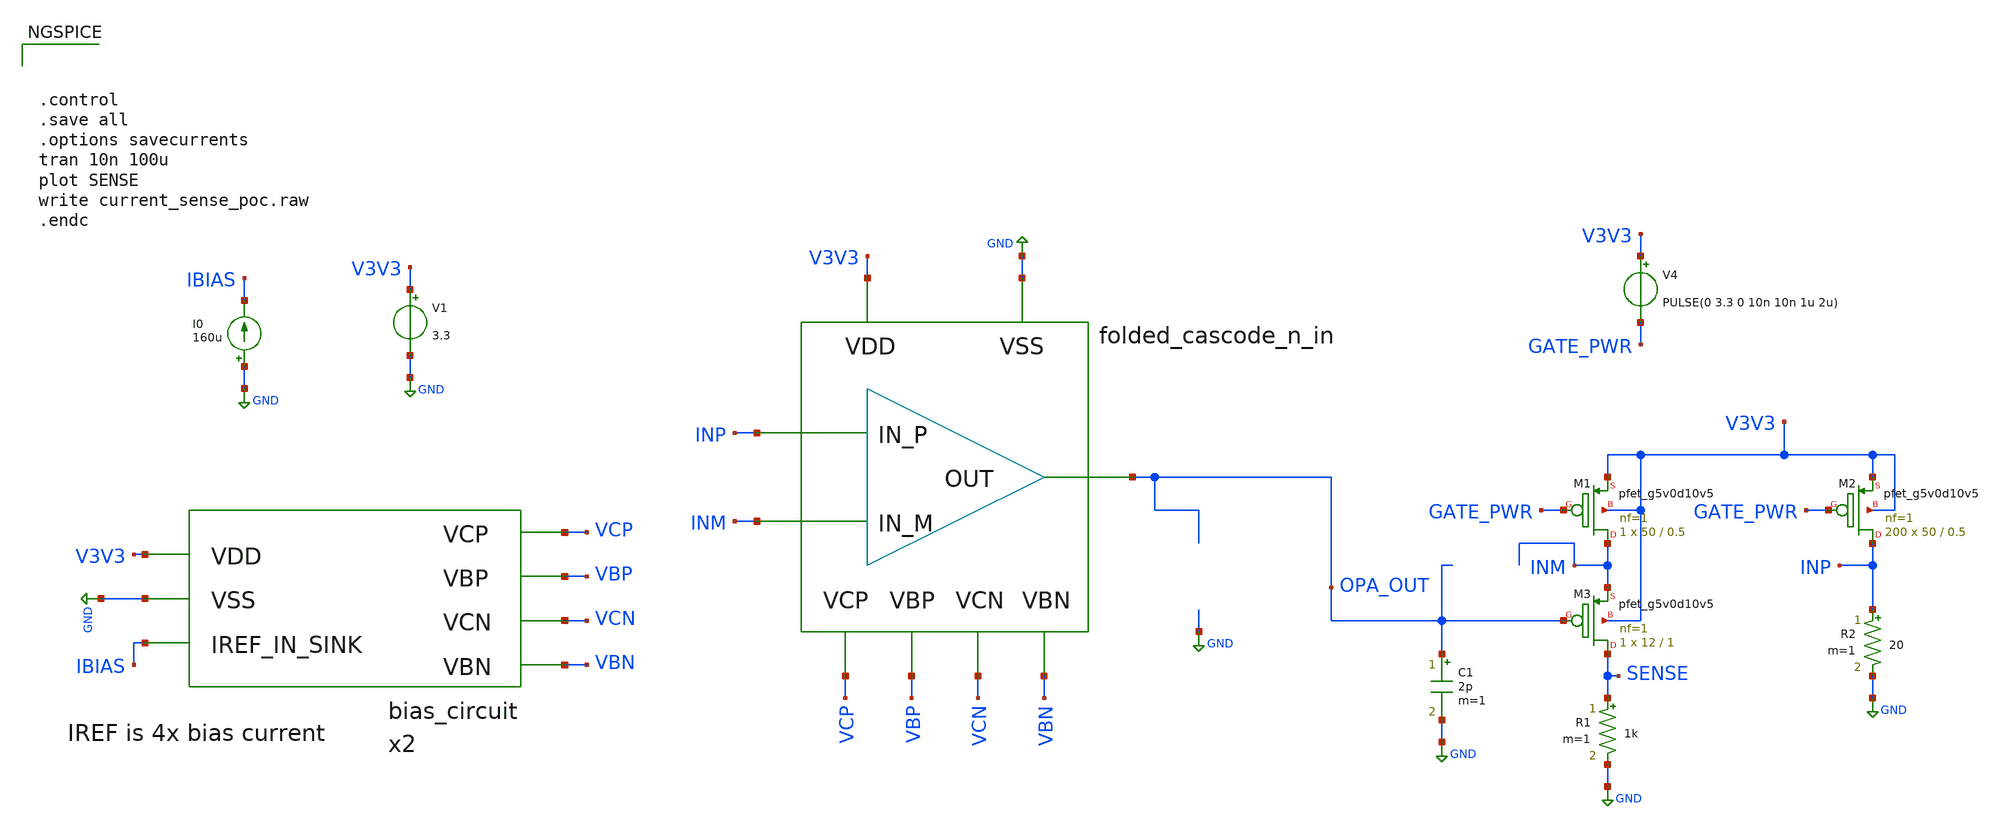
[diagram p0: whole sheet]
** sch_path: design/current-sense/current_sense_poc.sch
**.subckt current_sense_poc
V1 V3V3 GND 3.3
I0 GND IBIAS 160u
x2 V3V3 GND VCP VBP VCN VBN IBIAS bias_circuit
XM1 INM GATE_PWR V3V3 V3V3 sky130_fd_pr__pfet_g5v0d10v5 L=0.5 W=50 nf=1 ad='int((nf+1)/2) * W/nf * 0.29'
+ as='int((nf+2)/2) * W/nf * 0.29' pd='2*int((nf+1)/2) * (W/nf + 0.29)' ps='2*int((nf+2)/2) * (W/nf + 0.29)'
+ nrd='0.29 / W' nrs='0.29 / W' sa=0 sb=0 sd=0 mult=1 m=1
XM2 INP GATE_PWR V3V3 V3V3 sky130_fd_pr__pfet_g5v0d10v5 L=0.5 W=50 nf=1 ad='int((nf+1)/2) * W/nf * 0.29'
+ as='int((nf+2)/2) * W/nf * 0.29' pd='2*int((nf+1)/2) * (W/nf + 0.29)' ps='2*int((nf+2)/2) * (W/nf + 0.29)'
+ nrd='0.29 / W' nrs='0.29 / W' sa=0 sb=0 sd=0 mult=200 m=200
V4 V3V3 GATE_PWR PULSE(0 3.3 0 10n 10n 1u 2u)
XM3 SENSE OPA_OUT INM V3V3 sky130_fd_pr__pfet_g5v0d10v5 L=1 W=12 nf=1 ad='int((nf+1)/2) * W/nf * 0.29'
+ as='int((nf+2)/2) * W/nf * 0.29' pd='2*int((nf+1)/2) * (W/nf + 0.29)' ps='2*int((nf+2)/2) * (W/nf + 0.29)'
+ nrd='0.29 / W' nrs='0.29 / W' sa=0 sb=0 sd=0 mult=1 m=1
R1 SENSE GND 1k m=1
R2 INP GND 20 m=1
C1 OPA_OUT GND 2p m=1
**** begin user architecture code



.control
.save all
.options savecurrents
tran 10n 100u
plot SENSE
write current_sense_poc.raw
.endc



.include $::SKYWATER_MODELS/cells/nfet_01v8/sky130_fd_pr__nfet_01v8__tt.corner.spice
.include $::SKYWATER_MODELS/cells/nfet_01v8_lvt/sky130_fd_pr__nfet_01v8_lvt__tt.corner.spice
.include $::SKYWATER_MODELS/cells/pfet_01v8/sky130_fd_pr__pfet_01v8__tt.corner.spice
.include $::SKYWATER_MODELS/cells/nfet_03v3_nvt/sky130_fd_pr__nfet_03v3_nvt__tt.corner.spice
.include $::SKYWATER_MODELS/cells/nfet_05v0_nvt/sky130_fd_pr__nfet_05v0_nvt__tt.corner.spice
.include $::SKYWATER_MODELS/cells/esd_nfet_01v8/sky130_fd_pr__esd_nfet_01v8__tt.corner.spice
.include $::SKYWATER_MODELS/cells/pfet_01v8_lvt/sky130_fd_pr__pfet_01v8_lvt__tt.corner.spice
.include $::SKYWATER_MODELS/cells/pfet_01v8_hvt/sky130_fd_pr__pfet_01v8_hvt__tt.corner.spice
.include $::SKYWATER_MODELS/cells/esd_pfet_g5v0d10v5/sky130_fd_pr__esd_pfet_g5v0d10v5__tt.corner.spice
.include $::SKYWATER_MODELS/cells/pfet_g5v0d10v5/sky130_fd_pr__pfet_g5v0d10v5__tt.corner.spice
.include $::SKYWATER_MODELS/cells/pfet_g5v0d16v0/sky130_fd_pr__pfet_g5v0d16v0__tt.corner.spice
.include $::SKYWATER_MODELS/cells/nfet_g5v0d10v5/sky130_fd_pr__nfet_g5v0d10v5__tt.corner.spice
.include $::SKYWATER_MODELS/cells/nfet_g5v0d16v0/sky130_fd_pr__nfet_g5v0d16v0__tt_discrete.corner.spice
.include $::SKYWATER_MODELS/cells/esd_nfet_g5v0d10v5/sky130_fd_pr__esd_nfet_g5v0d10v5__tt.corner.spice
.include $::SKYWATER_MODELS/models/corners/tt/nonfet.spice
* Mismatch parameters
.include $::SKYWATER_MODELS/cells/nfet_01v8/sky130_fd_pr__nfet_01v8__mismatch.corner.spice
.include $::SKYWATER_MODELS/cells/pfet_01v8/sky130_fd_pr__pfet_01v8__mismatch.corner.spice
.include $::SKYWATER_MODELS/cells/nfet_01v8_lvt/sky130_fd_pr__nfet_01v8_lvt__mismatch.corner.spice
.include $::SKYWATER_MODELS/cells/pfet_01v8_lvt/sky130_fd_pr__pfet_01v8_lvt__mismatch.corner.spice
.include $::SKYWATER_MODELS/cells/pfet_01v8_hvt/sky130_fd_pr__pfet_01v8_hvt__mismatch.corner.spice
.include $::SKYWATER_MODELS/cells/nfet_g5v0d10v5/sky130_fd_pr__nfet_g5v0d10v5__mismatch.corner.spice
.include $::SKYWATER_MODELS/cells/pfet_g5v0d10v5/sky130_fd_pr__pfet_g5v0d10v5__mismatch.corner.spice
.include $::SKYWATER_MODELS/cells/nfet_05v0_nvt/sky130_fd_pr__nfet_05v0_nvt__mismatch.corner.spice
.include $::SKYWATER_MODELS/cells/nfet_03v3_nvt/sky130_fd_pr__nfet_03v3_nvt__mismatch.corner.spice
* Resistor$::SKYWATER_MODELS/Capacitor
.include $::SKYWATER_MODELS/models/r+c/res_typical__cap_typical.spice
.include $::SKYWATER_MODELS/models/r+c/res_typical__cap_typical__lin.spice
* Special cells
.include $::SKYWATER_MODELS/models/corners/tt/specialized_cells.spice
* All models
.include $::SKYWATER_MODELS/models/all.spice
* Corner
.include $::SKYWATER_MODELS/models/corners/tt/rf.spice

**** end user architecture code
**.ends

* expanding   symbol:  /home/wbraun/projects/open-pmic/design/bias-circuit/bias_circuit.sym # of
*+ pins=7
** sym_path: design/bias-circuit/bias_circuit.sym
** sch_path: design/bias-circuit/bias_circuit.sch
.subckt bias_circuit VDD VSS VCP VBP VCN VBN IREF_IN_SINK
*.ipin IREF_IN_SINK
*.ipin VCN
*.ipin VSS
*.ipin VDD
*.ipin VCP
*.ipin VBP
*.ipin VBN
XM2 VBP VBP VDD VDD sky130_fd_pr__pfet_g5v0d10v5 L=1 W=12 nf=1 ad='int((nf+1)/2) * W/nf * 0.29' as='int((nf+2)/2) * W/nf * 0.29'
+ pd='2*int((nf+1)/2) * (W/nf + 0.29)' ps='2*int((nf+2)/2) * (W/nf + 0.29)' nrd='0.29 / W' nrs='0.29 / W'
+ sa=0 sb=0 sd=0 mult=1 m=1
XM3 net1 VBP VDD VDD sky130_fd_pr__pfet_g5v0d10v5 L=5 W=12 nf=1 ad='int((nf+1)/2) * W/nf * 0.29' as='int((nf+2)/2) * W/nf * 0.29'
+ pd='2*int((nf+1)/2) * (W/nf + 0.29)' ps='2*int((nf+2)/2) * (W/nf + 0.29)' nrd='0.29 / W' nrs='0.29 / W'
+ sa=0 sb=0 sd=0 mult=1 m=1
XM4 VCN VBP VDD VDD sky130_fd_pr__pfet_g5v0d10v5 L=1 W=12 nf=1 ad='int((nf+1)/2) * W/nf * 0.29' as='int((nf+2)/2) * W/nf * 0.29'
+ pd='2*int((nf+1)/2) * (W/nf + 0.29)' ps='2*int((nf+2)/2) * (W/nf + 0.29)' nrd='0.29 / W' nrs='0.29 / W'
+ sa=0 sb=0 sd=0 mult=1 m=1
XM5 net1 net1 net2 VSS sky130_fd_pr__nfet_g5v0d10v5 L=1 W=12 nf=1 ad='int((nf+1)/2) * W/nf * 0.29' as='int((nf+2)/2) * W/nf * 0.29'
+ pd='2*int((nf+1)/2) * (W/nf + 0.29)' ps='2*int((nf+2)/2) * (W/nf + 0.29)' nrd='0.29 / W' nrs='0.29 / W'
+ sa=0 sb=0 sd=0 mult=4 m=4
XM6 net2 net1 VSS VSS sky130_fd_pr__nfet_g5v0d10v5 L=1 W=12 nf=1 ad='int((nf+1)/2) * W/nf * 0.29' as='int((nf+2)/2) * W/nf * 0.29'
+ pd='2*int((nf+1)/2) * (W/nf + 0.29)' ps='2*int((nf+2)/2) * (W/nf + 0.29)' nrd='0.29 / W' nrs='0.29 / W'
+ sa=0 sb=0 sd=0 mult=1 m=1
XM7 VCN VCN net2 VSS sky130_fd_pr__nfet_g5v0d10v5 L=1 W=12 nf=1 ad='int((nf+1)/2) * W/nf * 0.29' as='int((nf+2)/2) * W/nf * 0.29'
+ pd='2*int((nf+1)/2) * (W/nf + 0.29)' ps='2*int((nf+2)/2) * (W/nf + 0.29)' nrd='0.29 / W' nrs='0.29 / W'
+ sa=0 sb=0 sd=0 mult=1 m=1
XM8 VBN VBN VSS VSS sky130_fd_pr__nfet_g5v0d10v5 L=1 W=12 nf=1 ad='int((nf+1)/2) * W/nf * 0.29' as='int((nf+2)/2) * W/nf * 0.29'
+ pd='2*int((nf+1)/2) * (W/nf + 0.29)' ps='2*int((nf+2)/2) * (W/nf + 0.29)' nrd='0.29 / W' nrs='0.29 / W'
+ sa=0 sb=0 sd=0 mult=1 m=1
XM9 VBN VBP VDD VDD sky130_fd_pr__pfet_g5v0d10v5 L=1 W=12 nf=1 ad='int((nf+1)/2) * W/nf * 0.29' as='int((nf+2)/2) * W/nf * 0.29'
+ pd='2*int((nf+1)/2) * (W/nf + 0.29)' ps='2*int((nf+2)/2) * (W/nf + 0.29)' nrd='0.29 / W' nrs='0.29 / W'
+ sa=0 sb=0 sd=0 mult=1 m=1
XM10 net3 VBN VSS VSS sky130_fd_pr__nfet_g5v0d10v5 L=5 W=12 nf=1 ad='int((nf+1)/2) * W/nf * 0.29' as='int((nf+2)/2) * W/nf * 0.29'
+ pd='2*int((nf+1)/2) * (W/nf + 0.29)' ps='2*int((nf+2)/2) * (W/nf + 0.29)' nrd='0.29 / W' nrs='0.29 / W'
+ sa=0 sb=0 sd=0 mult=1 m=1
XM11 VCP VBN VSS VSS sky130_fd_pr__nfet_g5v0d10v5 L=1 W=12 nf=1 ad='int((nf+1)/2) * W/nf * 0.29' as='int((nf+2)/2) * W/nf * 0.29'
+ pd='2*int((nf+1)/2) * (W/nf + 0.29)' ps='2*int((nf+2)/2) * (W/nf + 0.29)' nrd='0.29 / W' nrs='0.29 / W'
+ sa=0 sb=0 sd=0 mult=1 m=1
XM12 net3 net3 net4 VDD sky130_fd_pr__pfet_g5v0d10v5 L=1 W=12 nf=1 ad='int((nf+1)/2) * W/nf * 0.29' as='int((nf+2)/2) * W/nf * 0.29'
+ pd='2*int((nf+1)/2) * (W/nf + 0.29)' ps='2*int((nf+2)/2) * (W/nf + 0.29)' nrd='0.29 / W' nrs='0.29 / W'
+ sa=0 sb=0 sd=0 mult=4 m=4
XM13 VCP VCP net4 VDD sky130_fd_pr__pfet_g5v0d10v5 L=1 W=12 nf=1 ad='int((nf+1)/2) * W/nf * 0.29' as='int((nf+2)/2) * W/nf * 0.29'
+ pd='2*int((nf+1)/2) * (W/nf + 0.29)' ps='2*int((nf+2)/2) * (W/nf + 0.29)' nrd='0.29 / W' nrs='0.29 / W'
+ sa=0 sb=0 sd=0 mult=1 m=1
XM14 net4 net3 VDD VDD sky130_fd_pr__pfet_g5v0d10v5 L=1 W=12 nf=1 ad='int((nf+1)/2) * W/nf * 0.29' as='int((nf+2)/2) * W/nf * 0.29'
+ pd='2*int((nf+1)/2) * (W/nf + 0.29)' ps='2*int((nf+2)/2) * (W/nf + 0.29)' nrd='0.29 / W' nrs='0.29 / W'
+ sa=0 sb=0 sd=0 mult=1 m=1
XM1 VBP IREF_IN_SINK VSS VSS sky130_fd_pr__nfet_g5v0d10v5 L=1 W=12 nf=1 ad='int((nf+1)/2) * W/nf * 0.29'
+ as='int((nf+2)/2) * W/nf * 0.29' pd='2*int((nf+1)/2) * (W/nf + 0.29)' ps='2*int((nf+2)/2) * (W/nf + 0.29)'
+ nrd='0.29 / W' nrs='0.29 / W' sa=0 sb=0 sd=0 mult=1 m=1
XM15 IREF_IN_SINK IREF_IN_SINK VSS VSS sky130_fd_pr__nfet_g5v0d10v5 L=1 W=12 nf=1 ad='int((nf+1)/2) * W/nf * 0.29'
+ as='int((nf+2)/2) * W/nf * 0.29' pd='2*int((nf+1)/2) * (W/nf + 0.29)' ps='2*int((nf+2)/2) * (W/nf + 0.29)'
+ nrd='0.29 / W' nrs='0.29 / W' sa=0 sb=0 sd=0 mult=4 m=4
.ends

.GLOBAL GND
**** begin user architecture code
[sky130_models]
**** end user architecture code
.end
